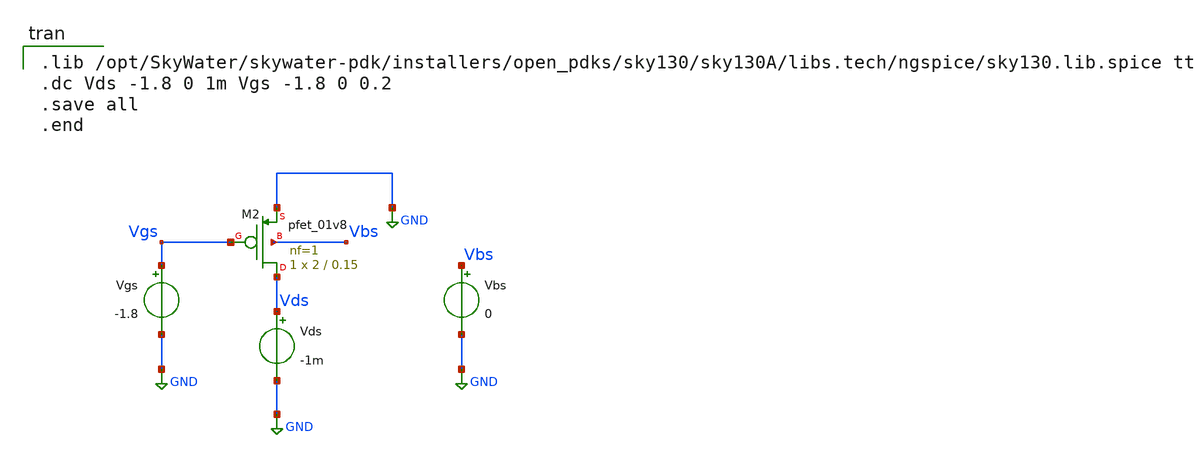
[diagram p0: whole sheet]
** sch_path: 1/xschem/pmos_test.sch
**.subckt pmos_test
Vds Vds GND -1m
.save i(vds)
Vgs Vgs GND -1.8
.save i(vgs)
Vbs Vbs GND 0
.save i(vbs)
XM2 Vds Vgs GND Vbs sky130_fd_pr__pfet_01v8 L=0.15 W=2 nf=1 ad='int((1 + 1)/2) * 2 / 1 * 0.29' as='int((1 + 2)/2) * 2 / 1 * 0.29'
+ pd='2*int((1 + 1)/2) * (2 / 1 + 0.29)' ps='2*int((1 + 2)/2) * (2 / 1 + 0.29)' nrd='0.29 / 2 ' nrs='0.29 / 2 '
+ sa=0 sb=0 sd=0 mult=1 m=1
**** begin user architecture code

.lib /opt/SkyWater/skywater-pdk/installers/open_pdks/sky130/sky130A/libs.tech/ngspice/sky130.lib.spice tt
.dc Vds -1.8 0 1m Vgs -1.8 0 0.2
.save all
.end

**** end user architecture code
**.ends
.GLOBAL GND
.end
